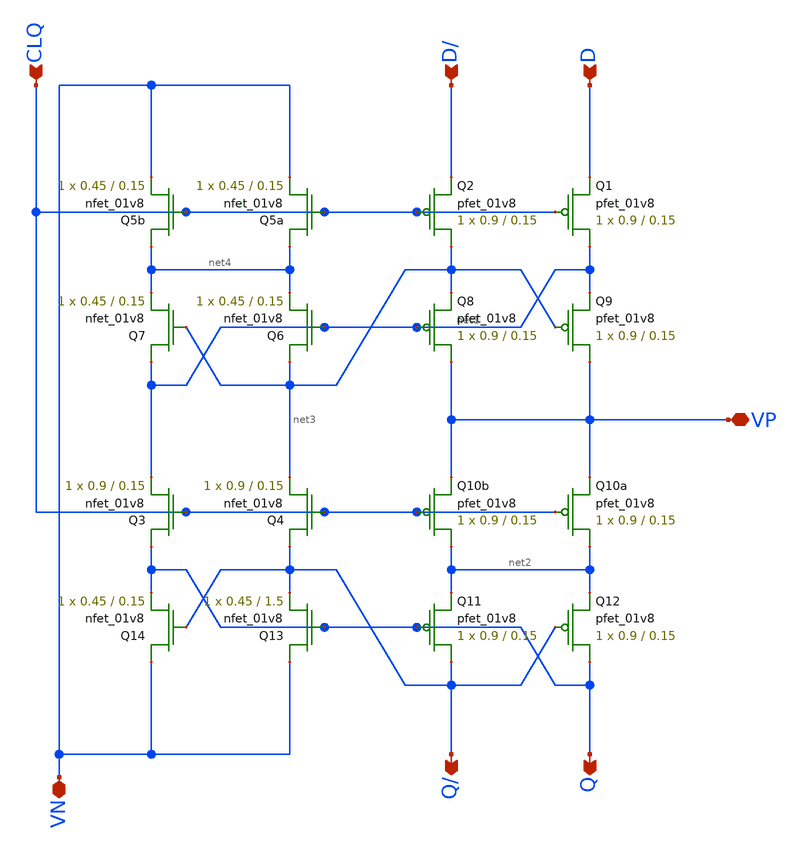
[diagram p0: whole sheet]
** sch_path: MADVLSI_MP2/Lay_CSRL_4_Pin.sch
**.subckt Lay_CSRL_4_Pin D/ D CLQ VP VN Q/ Q
*.ipin D/
*.ipin D
*.ipin CLQ
*.iopin VP
*.iopin VN
*.opin Q/
*.opin Q
XQ2 net3 CLQ D/ VDD sky130_fd_pr__pfet_01v8 L=0.15 W=0.9 nf=1 ad='int((nf+1)/2) * W/nf * 0.29' as='int((nf+2)/2) * W/nf * 0.29'
+ pd='2*int((nf+1)/2) * (W/nf + 0.29)' ps='2*int((nf+2)/2) * (W/nf + 0.29)' nrd='0.29 / W' nrs='0.29 / W'
+ sa=0 sb=0 sd=0 mult=1 m=1
XQ8 VP net1 net3 VDD sky130_fd_pr__pfet_01v8 L=0.15 W=0.9 nf=1 ad='int((nf+1)/2) * W/nf * 0.29' as='int((nf+2)/2) * W/nf * 0.29'
+ pd='2*int((nf+1)/2) * (W/nf + 0.29)' ps='2*int((nf+2)/2) * (W/nf + 0.29)' nrd='0.29 / W' nrs='0.29 / W'
+ sa=0 sb=0 sd=0 mult=1 m=1
XQ10b net2 CLQ VP VDD sky130_fd_pr__pfet_01v8 L=0.15 W=0.9 nf=1 ad='int((nf+1)/2) * W/nf * 0.29' as='int((nf+2)/2) * W/nf * 0.29'
+ pd='2*int((nf+1)/2) * (W/nf + 0.29)' ps='2*int((nf+2)/2) * (W/nf + 0.29)' nrd='0.29 / W' nrs='0.29 / W'
+ sa=0 sb=0 sd=0 mult=1 m=1
XQ11 Q/ Q net2 VDD sky130_fd_pr__pfet_01v8 L=0.15 W=0.9 nf=1 ad='int((nf+1)/2) * W/nf * 0.29' as='int((nf+2)/2) * W/nf * 0.29'
+ pd='2*int((nf+1)/2) * (W/nf + 0.29)' ps='2*int((nf+2)/2) * (W/nf + 0.29)' nrd='0.29 / W' nrs='0.29 / W'
+ sa=0 sb=0 sd=0 mult=1 m=1
XQ1 net1 CLQ D VDD sky130_fd_pr__pfet_01v8 L=0.15 W=0.9 nf=1 ad='int((nf+1)/2) * W/nf * 0.29' as='int((nf+2)/2) * W/nf * 0.29'
+ pd='2*int((nf+1)/2) * (W/nf + 0.29)' ps='2*int((nf+2)/2) * (W/nf + 0.29)' nrd='0.29 / W' nrs='0.29 / W'
+ sa=0 sb=0 sd=0 mult=1 m=1
XQ9 VP net3 net1 VDD sky130_fd_pr__pfet_01v8 L=0.15 W=0.9 nf=1 ad='int((nf+1)/2) * W/nf * 0.29' as='int((nf+2)/2) * W/nf * 0.29'
+ pd='2*int((nf+1)/2) * (W/nf + 0.29)' ps='2*int((nf+2)/2) * (W/nf + 0.29)' nrd='0.29 / W' nrs='0.29 / W'
+ sa=0 sb=0 sd=0 mult=1 m=1
XQ10a net2 CLQ VP VDD sky130_fd_pr__pfet_01v8 L=0.15 W=0.9 nf=1 ad='int((nf+1)/2) * W/nf * 0.29' as='int((nf+2)/2) * W/nf * 0.29'
+ pd='2*int((nf+1)/2) * (W/nf + 0.29)' ps='2*int((nf+2)/2) * (W/nf + 0.29)' nrd='0.29 / W' nrs='0.29 / W'
+ sa=0 sb=0 sd=0 mult=1 m=1
XQ12 Q Q/ net2 VDD sky130_fd_pr__pfet_01v8 L=0.15 W=0.9 nf=1 ad='int((nf+1)/2) * W/nf * 0.29' as='int((nf+2)/2) * W/nf * 0.29'
+ pd='2*int((nf+1)/2) * (W/nf + 0.29)' ps='2*int((nf+2)/2) * (W/nf + 0.29)' nrd='0.29 / W' nrs='0.29 / W'
+ sa=0 sb=0 sd=0 mult=1 m=1
XQ5a net4 CLQ VN GND sky130_fd_pr__nfet_01v8 L=0.15 W=0.45 nf=1 ad='int((nf+1)/2) * W/nf * 0.29' as='int((nf+2)/2) * W/nf * 0.29'
+ pd='2*int((nf+1)/2) * (W/nf + 0.29)' ps='2*int((nf+2)/2) * (W/nf + 0.29)' nrd='0.29 / W' nrs='0.29 / W'
+ sa=0 sb=0 sd=0 mult=1 m=1
XQ6 net3 net1 net4 GND sky130_fd_pr__nfet_01v8 L=0.15 W=0.45 nf=1 ad='int((nf+1)/2) * W/nf * 0.29' as='int((nf+2)/2) * W/nf * 0.29'
+ pd='2*int((nf+1)/2) * (W/nf + 0.29)' ps='2*int((nf+2)/2) * (W/nf + 0.29)' nrd='0.29 / W' nrs='0.29 / W'
+ sa=0 sb=0 sd=0 mult=1 m=1
XQ4 Q/ CLQ net3 GND sky130_fd_pr__nfet_01v8 L=0.15 W=0.9 nf=1 ad='int((nf+1)/2) * W/nf * 0.29' as='int((nf+2)/2) * W/nf * 0.29'
+ pd='2*int((nf+1)/2) * (W/nf + 0.29)' ps='2*int((nf+2)/2) * (W/nf + 0.29)' nrd='0.29 / W' nrs='0.29 / W'
+ sa=0 sb=0 sd=0 mult=1 m=1
XQ13 VN Q Q/ GND sky130_fd_pr__nfet_01v8 L=1.5 W=0.45 nf=1 ad='int((nf+1)/2) * W/nf * 0.29' as='int((nf+2)/2) * W/nf * 0.29'
+ pd='2*int((nf+1)/2) * (W/nf + 0.29)' ps='2*int((nf+2)/2) * (W/nf + 0.29)' nrd='0.29 / W' nrs='0.29 / W'
+ sa=0 sb=0 sd=0 mult=1 m=1
XQ5b net4 CLQ VN GND sky130_fd_pr__nfet_01v8 L=0.15 W=0.45 nf=1 ad='int((nf+1)/2) * W/nf * 0.29' as='int((nf+2)/2) * W/nf * 0.29'
+ pd='2*int((nf+1)/2) * (W/nf + 0.29)' ps='2*int((nf+2)/2) * (W/nf + 0.29)' nrd='0.29 / W' nrs='0.29 / W'
+ sa=0 sb=0 sd=0 mult=1 m=1
XQ7 net1 net3 net4 GND sky130_fd_pr__nfet_01v8 L=0.15 W=0.45 nf=1 ad='int((nf+1)/2) * W/nf * 0.29' as='int((nf+2)/2) * W/nf * 0.29'
+ pd='2*int((nf+1)/2) * (W/nf + 0.29)' ps='2*int((nf+2)/2) * (W/nf + 0.29)' nrd='0.29 / W' nrs='0.29 / W'
+ sa=0 sb=0 sd=0 mult=1 m=1
XQ3 Q CLQ net1 GND sky130_fd_pr__nfet_01v8 L=0.15 W=0.9 nf=1 ad='int((nf+1)/2) * W/nf * 0.29' as='int((nf+2)/2) * W/nf * 0.29'
+ pd='2*int((nf+1)/2) * (W/nf + 0.29)' ps='2*int((nf+2)/2) * (W/nf + 0.29)' nrd='0.29 / W' nrs='0.29 / W'
+ sa=0 sb=0 sd=0 mult=1 m=1
XQ14 VN Q/ Q GND sky130_fd_pr__nfet_01v8 L=0.15 W=0.45 nf=1 ad='int((nf+1)/2) * W/nf * 0.29' as='int((nf+2)/2) * W/nf * 0.29'
+ pd='2*int((nf+1)/2) * (W/nf + 0.29)' ps='2*int((nf+2)/2) * (W/nf + 0.29)' nrd='0.29 / W' nrs='0.29 / W'
+ sa=0 sb=0 sd=0 mult=1 m=1
**.ends
.end
